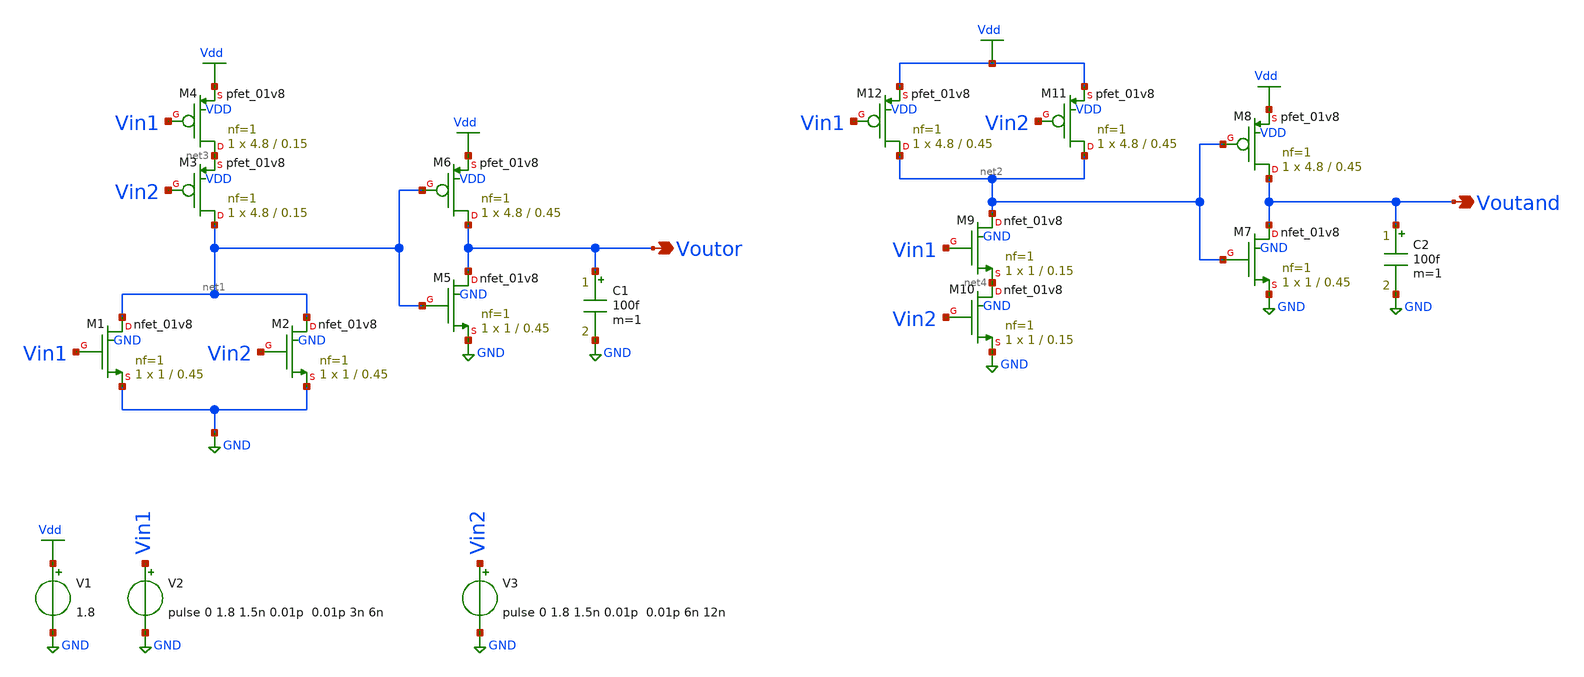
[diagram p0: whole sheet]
** sch_path: Circuiti/porta-and-or.sch
**.subckt porta-and-or Voutor Voutand
*.opin Voutor
*.opin Voutand
XM1 net1 Vin1 GND GND sky130_fd_pr__nfet_01v8 L=0.45 W=1 nf=1 ad='int((nf+1)/2) * W/nf * 0.29' as='int((nf+2)/2) * W/nf * 0.29'
+ pd='2*int((nf+1)/2) * (W/nf + 0.29)' ps='2*int((nf+2)/2) * (W/nf + 0.29)' nrd='0.29 / W' nrs='0.29 / W'
+ sa=0 sb=0 sd=0 mult=1 m=1
V1 Vdd GND 1.8
XM3 net1 Vin2 net3 VDD sky130_fd_pr__pfet_01v8 L=0.15 W=4.8 nf=1 ad='int((nf+1)/2) * W/nf * 0.29' as='int((nf+2)/2) * W/nf * 0.29'
+ pd='2*int((nf+1)/2) * (W/nf + 0.29)' ps='2*int((nf+2)/2) * (W/nf + 0.29)' nrd='0.29 / W' nrs='0.29 / W'
+ sa=0 sb=0 sd=0 mult=1 m=1
V2 Vin1 GND pulse 0 1.8 1.5n 0.01p 0.01p 3n 6n
C1 Voutor GND 100f m=1
XM4 net3 Vin1 Vdd VDD sky130_fd_pr__pfet_01v8 L=0.15 W=4.8 nf=1 ad='int((nf+1)/2) * W/nf * 0.29' as='int((nf+2)/2) * W/nf * 0.29'
+ pd='2*int((nf+1)/2) * (W/nf + 0.29)' ps='2*int((nf+2)/2) * (W/nf + 0.29)' nrd='0.29 / W' nrs='0.29 / W'
+ sa=0 sb=0 sd=0 mult=1 m=1
XM2 net1 Vin2 GND GND sky130_fd_pr__nfet_01v8 L=0.45 W=1 nf=1 ad='int((nf+1)/2) * W/nf * 0.29' as='int((nf+2)/2) * W/nf * 0.29'
+ pd='2*int((nf+1)/2) * (W/nf + 0.29)' ps='2*int((nf+2)/2) * (W/nf + 0.29)' nrd='0.29 / W' nrs='0.29 / W'
+ sa=0 sb=0 sd=0 mult=1 m=1
V3 Vin2 GND pulse 0 1.8 1.5n 0.01p 0.01p 6n 12n
XM5 Voutor net1 GND GND sky130_fd_pr__nfet_01v8 L=0.45 W=1 nf=1 ad='int((nf+1)/2) * W/nf * 0.29' as='int((nf+2)/2) * W/nf * 0.29'
+ pd='2*int((nf+1)/2) * (W/nf + 0.29)' ps='2*int((nf+2)/2) * (W/nf + 0.29)' nrd='0.29 / W' nrs='0.29 / W'
+ sa=0 sb=0 sd=0 mult=1 m=1
XM6 Voutor net1 Vdd VDD sky130_fd_pr__pfet_01v8 L=0.45 W=4.8 nf=1 ad='int((nf+1)/2) * W/nf * 0.29' as='int((nf+2)/2) * W/nf * 0.29'
+ pd='2*int((nf+1)/2) * (W/nf + 0.29)' ps='2*int((nf+2)/2) * (W/nf + 0.29)' nrd='0.29 / W' nrs='0.29 / W'
+ sa=0 sb=0 sd=0 mult=1 m=1
XM7 Voutand net2 GND GND sky130_fd_pr__nfet_01v8 L=0.45 W=1 nf=1 ad='int((nf+1)/2) * W/nf * 0.29' as='int((nf+2)/2) * W/nf * 0.29'
+ pd='2*int((nf+1)/2) * (W/nf + 0.29)' ps='2*int((nf+2)/2) * (W/nf + 0.29)' nrd='0.29 / W' nrs='0.29 / W'
+ sa=0 sb=0 sd=0 mult=1 m=1
XM8 Voutand net2 Vdd VDD sky130_fd_pr__pfet_01v8 L=0.45 W=4.8 nf=1 ad='int((nf+1)/2) * W/nf * 0.29' as='int((nf+2)/2) * W/nf * 0.29'
+ pd='2*int((nf+1)/2) * (W/nf + 0.29)' ps='2*int((nf+2)/2) * (W/nf + 0.29)' nrd='0.29 / W' nrs='0.29 / W'
+ sa=0 sb=0 sd=0 mult=1 m=1
XM11 net2 Vin2 Vdd VDD sky130_fd_pr__pfet_01v8 L=0.45 W=4.8 nf=1 ad='int((nf+1)/2) * W/nf * 0.29' as='int((nf+2)/2) * W/nf * 0.29'
+ pd='2*int((nf+1)/2) * (W/nf + 0.29)' ps='2*int((nf+2)/2) * (W/nf + 0.29)' nrd='0.29 / W' nrs='0.29 / W'
+ sa=0 sb=0 sd=0 mult=1 m=1
XM12 net2 Vin1 Vdd VDD sky130_fd_pr__pfet_01v8 L=0.45 W=4.8 nf=1 ad='int((nf+1)/2) * W/nf * 0.29' as='int((nf+2)/2) * W/nf * 0.29'
+ pd='2*int((nf+1)/2) * (W/nf + 0.29)' ps='2*int((nf+2)/2) * (W/nf + 0.29)' nrd='0.29 / W' nrs='0.29 / W'
+ sa=0 sb=0 sd=0 mult=1 m=1
XM9 net2 Vin1 net4 GND sky130_fd_pr__nfet_01v8 L=0.15 W=1 nf=1 ad='int((nf+1)/2) * W/nf * 0.29' as='int((nf+2)/2) * W/nf * 0.29'
+ pd='2*int((nf+1)/2) * (W/nf + 0.29)' ps='2*int((nf+2)/2) * (W/nf + 0.29)' nrd='0.29 / W' nrs='0.29 / W'
+ sa=0 sb=0 sd=0 mult=1 m=1
XM10 net4 Vin2 GND GND sky130_fd_pr__nfet_01v8 L=0.15 W=1 nf=1 ad='int((nf+1)/2) * W/nf * 0.29' as='int((nf+2)/2) * W/nf * 0.29'
+ pd='2*int((nf+1)/2) * (W/nf + 0.29)' ps='2*int((nf+2)/2) * (W/nf + 0.29)' nrd='0.29 / W' nrs='0.29 / W'
+ sa=0 sb=0 sd=0 mult=1 m=1
C2 Voutand GND 100f m=1
**** begin user architecture code


.lib /home/matteo/xschem_downloads/skywater-pdk/libraries/sky130_fd_pr_ngspice/latest/models/sky130.lib.spice tt

*.include /home/matteo/xschem_downloads/skywater-pdk/libraries/sky130_fd_pr_ngspice/latest/cells/nfet_01v8/sky130_fd_pr__nfet_01v8__tt.corner.spice

.param mc_mm_switch=0
.param mc_pr_switch=1



.control
tran 0.05n 18n
plot vin1 vin2+2 voutor+4 voutand+6
wrdata output.txt vin1 vin2 voutor voutand
.endc


**** end user architecture code
**.ends
.GLOBAL Vdd
.GLOBAL GND
.end
